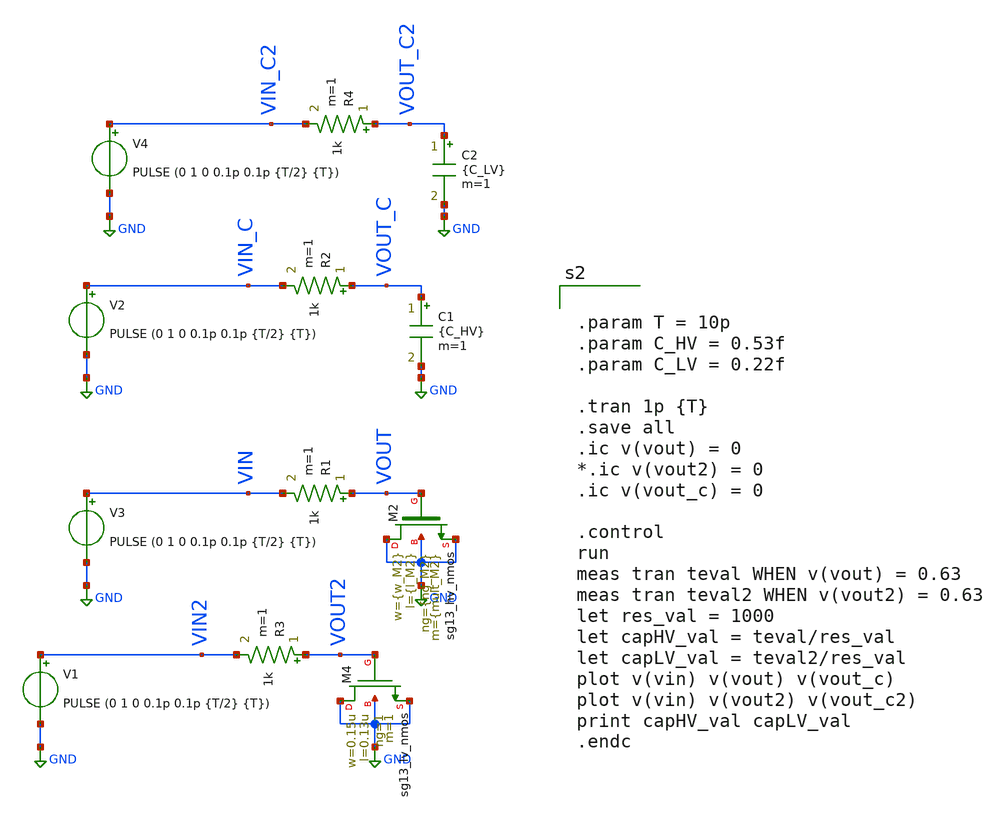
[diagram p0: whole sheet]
** sch_path: xschem/DCDCBuck/TB_hvNMOS_cgate_ext.sch
**.subckt TB_hvNMOS_cgate_ext
R1 VOUT VIN 1k m=1
XM2 GND VOUT GND GND sg13_hv_nmos w={w_M2} l={l_M2} ng={ng_M2} m={mult_M2} mm_ok=1
R2 VOUT_C VIN_C 1k m=1
V2 VIN_C GND PULSE (0 1 0 0.1p 0.1p {T/2} {T})
C1 VOUT_C GND {C_HV} m=1
V3 VIN GND PULSE (0 1 0 0.1p 0.1p {T/2} {T})
R3 VOUT2 VIN2 1k m=1
V1 VIN2 GND PULSE (0 1 0 0.1p 0.1p {T/2} {T})
XM4 GND VOUT2 GND GND sg13_lv_nmos w=0.15u l=0.13u ng=1 m=1 mm_ok=1
R4 VOUT_C2 VIN_C2 1k m=1
V4 VIN_C2 GND PULSE (0 1 0 0.1p 0.1p {T/2} {T})
C2 VOUT_C2 GND {C_LV} m=1
**** begin user architecture code


.param T = 10p
.param C_HV = 0.53f
.param C_LV = 0.22f

.tran 1p {T}
.save all
.ic v(vout) = 0
*.ic v(vout2) = 0
.ic v(vout_c) = 0

.control
run
meas tran teval WHEN v(vout) = 0.63
meas tran teval2 WHEN v(vout2) = 0.63
let res_val = 1000
let capHV_val = teval/res_val
let capLV_val = teval2/res_val
plot v(vin) v(vout) v(vout_c)
plot v(vin) v(vout2) v(vout_c2)
print capHV_val capLV_val
.endc




.param mult = 1
.param temp=27
.param mult_M1 = 3*mult
.param w_M1 =0.3u
.param l_M1 = 0.45u
.param ng_M1 = 1

.param mult_M2 = 1*mult
.param w_M2 =0.3u
.param l_M2 =0.45u
.param ng_M2 =1







.lib cornerMOShv.lib mos_tt
.lib cornerMOSlv.lib mos_tt
*.lib cornerMOShv.lib mos_ff
*.lib cornerMOSlv.lib mos_ff
*.lib cornerMOShv.lib mos_ss
*.lib cornerMOSlv.lib mos_ss
*.lib cornerMOShv.lib mos_sf
*.lib cornerMOSlv.lib mos_sf
*.lib cornerMOShv.lib mos_fs
*.lib cornerMOSlv.lib mos_fs

*.include /opt/pdks/ihp-sg13g2/libs.ref/sg13g2_stdcell/spice/sg13g2_stdcell.spice
*.lib $::SG13G2_MODELS/cornerRES.lib res_typ
*.lib $::SG13G2_MODELS/cornerCAP.lib cap_typ
*.lib $::SG13G2_MODELS/diodes.lib

**** end user architecture code
**.ends
.GLOBAL GND
.end
